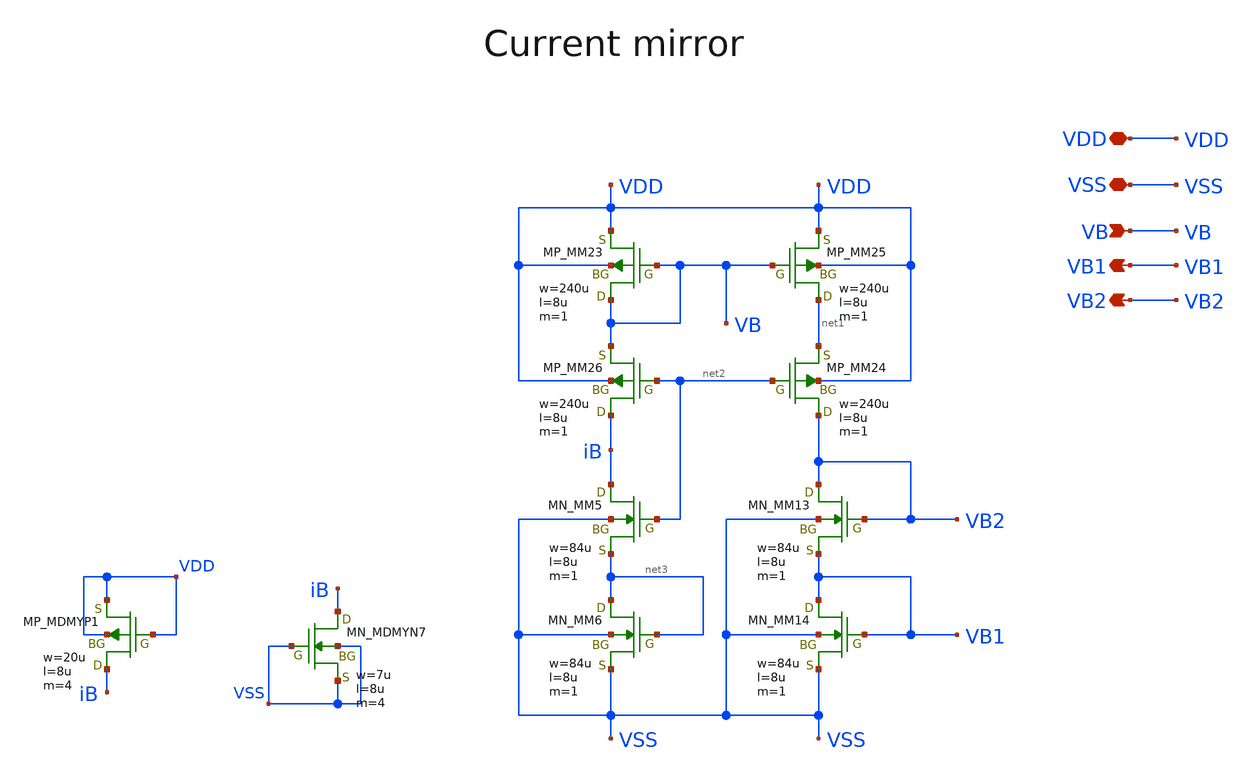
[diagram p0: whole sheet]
** sch_path: member_project/AM_Radio/noritsuna/xschem/current_mirror.sch
**.subckt current_mirror VDD VSS VB VB1 VB2
*.iopin VDD
*.iopin VSS
*.ipin VB
*.opin VB1
*.opin VB2
MM13 VB2 VB2 VB1 VSS NMOS w=84u l=8u as=0 ad=0 ps=0 pd=0 nrd=0 nrs=0 m=1
MM14 VB1 VB1 VSS VSS NMOS w=84u l=8u as=0 ad=0 ps=0 pd=0 nrd=0 nrs=0 m=1
MM23 VB VB VDD VDD PMOS w=240u l=8u as=0 ad=0 ps=0 pd=0 nrd=0 nrs=0 m=1
MM24 VB2 net2 net1 VDD PMOS w=240u l=8u as=0 ad=0 ps=0 pd=0 nrd=0 nrs=0 m=1
MM25 net1 VB VDD VDD PMOS w=240u l=8u as=0 ad=0 ps=0 pd=0 nrd=0 nrs=0 m=1
MM26 iB net2 VB VDD PMOS w=240u l=8u as=0 ad=0 ps=0 pd=0 nrd=0 nrs=0 m=1
MM5 iB net2 net3 VSS NMOS w=84u l=8u as=0 ad=0 ps=0 pd=0 nrd=0 nrs=0 m=1
MM6 net3 net3 VSS VSS NMOS w=84u l=8u as=0 ad=0 ps=0 pd=0 nrd=0 nrs=0 m=1
XMDMYP1 iB VDD VDD VDD PMOS w=20u l=8u as=0 ad=0 ps=0 pd=0 nrd=0 nrs=0 m=4
XMDMYN7 iB VSS VSS VSS NMOS w=7u l=8u as=0 ad=0 ps=0 pd=0 nrd=0 nrs=0 m=4
**.ends
.end
